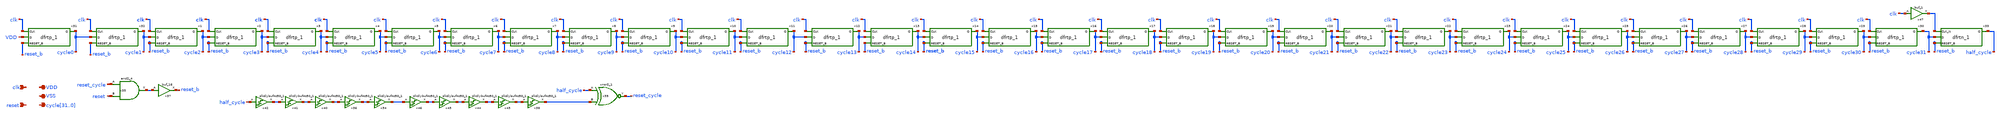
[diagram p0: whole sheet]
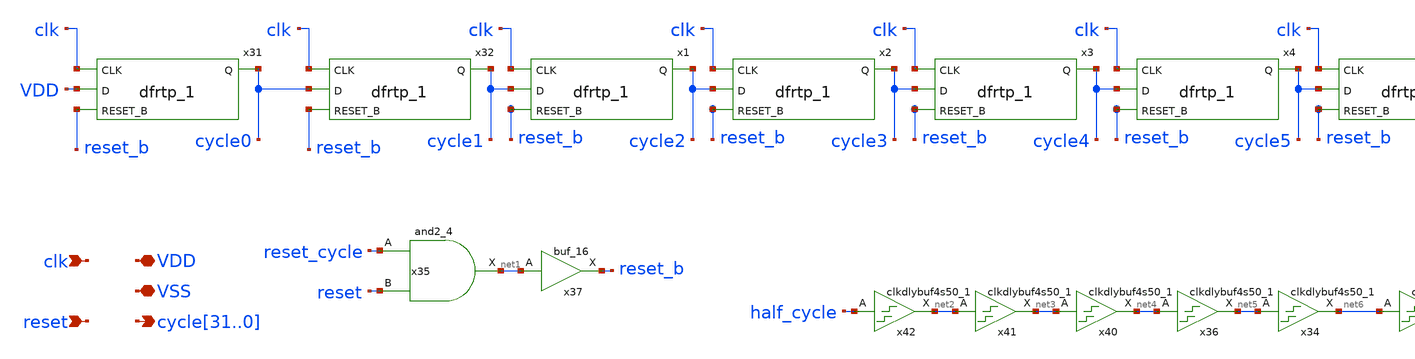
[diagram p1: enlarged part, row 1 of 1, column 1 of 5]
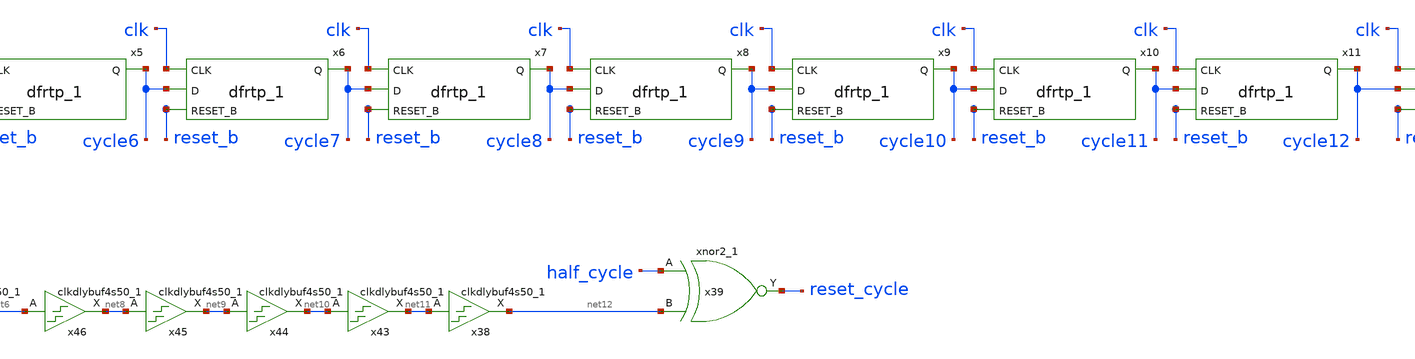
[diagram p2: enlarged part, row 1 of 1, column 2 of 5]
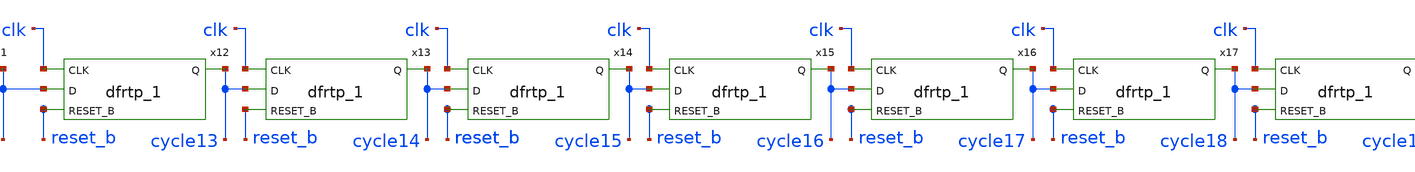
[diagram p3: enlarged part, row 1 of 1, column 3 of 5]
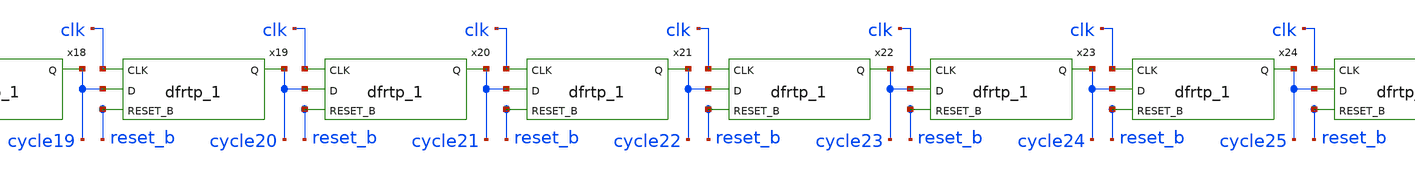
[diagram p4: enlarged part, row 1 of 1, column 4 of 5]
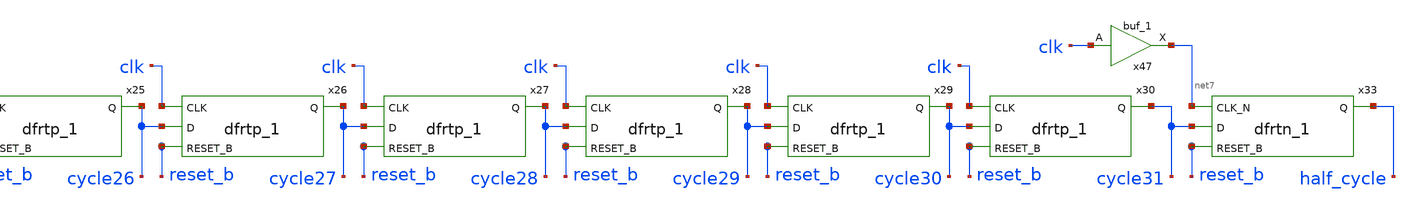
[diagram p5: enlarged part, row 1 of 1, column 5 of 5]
** sch_path: xschem/src/shifted_clock_generator/shifted_clock_generator.sch
**.subckt shifted_clock_generator
*+ cycle31,cycle30,cycle29,cycle28,cycle27,cycle26,cycle25,cycle24,cycle23,cycle22,cycle21,cycle20,cycle19,cycle18,cycle17,cycle16,cycle15,cycle14,cycle13,cycle12,cycle11,cycle10,cycle9,cycle8,cycle7,cycle6,cycle5,cycle4,cycle3,cycle2,cycle1,cycle0 VSS VDD clk reset
*.opin
*+ cycle31,cycle30,cycle29,cycle28,cycle27,cycle26,cycle25,cycle24,cycle23,cycle22,cycle21,cycle20,cycle19,cycle18,cycle17,cycle16,cycle15,cycle14,cycle13,cycle12,cycle11,cycle10,cycle9,cycle8,cycle7,cycle6,cycle5,cycle4,cycle3,cycle2,cycle1,cycle0
*.iopin VSS
*.iopin VDD
*.ipin clk
*.ipin reset
x32 clk cycle0 reset_b VSS VSS VDD VDD cycle1 sky130_fd_sc_hd__dfrtp_1
x1 clk cycle1 reset_b VSS VSS VDD VDD cycle2 sky130_fd_sc_hd__dfrtp_1
x2 clk cycle2 reset_b VSS VSS VDD VDD cycle3 sky130_fd_sc_hd__dfrtp_1
x3 clk cycle3 reset_b VSS VSS VDD VDD cycle4 sky130_fd_sc_hd__dfrtp_1
x4 clk cycle4 reset_b VSS VSS VDD VDD cycle5 sky130_fd_sc_hd__dfrtp_1
x5 clk cycle5 reset_b VSS VSS VDD VDD cycle6 sky130_fd_sc_hd__dfrtp_1
x6 clk cycle6 reset_b VSS VSS VDD VDD cycle7 sky130_fd_sc_hd__dfrtp_1
x7 clk cycle7 reset_b VSS VSS VDD VDD cycle8 sky130_fd_sc_hd__dfrtp_1
x8 clk cycle8 reset_b VSS VSS VDD VDD cycle9 sky130_fd_sc_hd__dfrtp_1
x9 clk cycle9 reset_b VSS VSS VDD VDD cycle10 sky130_fd_sc_hd__dfrtp_1
x10 clk cycle10 reset_b VSS VSS VDD VDD cycle11 sky130_fd_sc_hd__dfrtp_1
x11 clk cycle11 reset_b VSS VSS VDD VDD cycle12 sky130_fd_sc_hd__dfrtp_1
x12 clk cycle12 reset_b VSS VSS VDD VDD cycle13 sky130_fd_sc_hd__dfrtp_1
x13 clk cycle13 reset_b VSS VSS VDD VDD cycle14 sky130_fd_sc_hd__dfrtp_1
x14 clk cycle14 reset_b VSS VSS VDD VDD cycle15 sky130_fd_sc_hd__dfrtp_1
x15 clk cycle15 reset_b VSS VSS VDD VDD cycle16 sky130_fd_sc_hd__dfrtp_1
x16 clk cycle16 reset_b VSS VSS VDD VDD cycle17 sky130_fd_sc_hd__dfrtp_1
x17 clk cycle17 reset_b VSS VSS VDD VDD cycle18 sky130_fd_sc_hd__dfrtp_1
x18 clk cycle18 reset_b VSS VSS VDD VDD cycle19 sky130_fd_sc_hd__dfrtp_1
x19 clk cycle19 reset_b VSS VSS VDD VDD cycle20 sky130_fd_sc_hd__dfrtp_1
x20 clk cycle20 reset_b VSS VSS VDD VDD cycle21 sky130_fd_sc_hd__dfrtp_1
x21 clk cycle21 reset_b VSS VSS VDD VDD cycle22 sky130_fd_sc_hd__dfrtp_1
x22 clk cycle22 reset_b VSS VSS VDD VDD cycle23 sky130_fd_sc_hd__dfrtp_1
x23 clk cycle23 reset_b VSS VSS VDD VDD cycle24 sky130_fd_sc_hd__dfrtp_1
x24 clk cycle24 reset_b VSS VSS VDD VDD cycle25 sky130_fd_sc_hd__dfrtp_1
x25 clk cycle25 reset_b VSS VSS VDD VDD cycle26 sky130_fd_sc_hd__dfrtp_1
x26 clk cycle26 reset_b VSS VSS VDD VDD cycle27 sky130_fd_sc_hd__dfrtp_1
x27 clk cycle27 reset_b VSS VSS VDD VDD cycle28 sky130_fd_sc_hd__dfrtp_1
x28 clk cycle28 reset_b VSS VSS VDD VDD cycle29 sky130_fd_sc_hd__dfrtp_1
x29 clk cycle29 reset_b VSS VSS VDD VDD cycle30 sky130_fd_sc_hd__dfrtp_1
x30 clk cycle30 reset_b VSS VSS VDD VDD cycle31 sky130_fd_sc_hd__dfrtp_1
x31 clk VDD reset_b VSS VSS VDD VDD cycle0 sky130_fd_sc_hd__dfrtp_1
x37 net1 VSS VSS VDD VDD reset_b sky130_fd_sc_hd__buf_16
x35 reset_cycle reset VSS VSS VDD VDD net1 sky130_fd_sc_hd__and2_4
x34 net5 VSS VSS VDD VDD net6 sky130_fd_sc_hd__clkdlybuf4s50_1
x39 half_cycle net12 VSS VSS VDD VDD reset_cycle sky130_fd_sc_hd__xnor2_1
x36 net4 VSS VSS VDD VDD net5 sky130_fd_sc_hd__clkdlybuf4s50_1
x40 net3 VSS VSS VDD VDD net4 sky130_fd_sc_hd__clkdlybuf4s50_1
x41 net2 VSS VSS VDD VDD net3 sky130_fd_sc_hd__clkdlybuf4s50_1
x42 half_cycle VSS VSS VDD VDD net2 sky130_fd_sc_hd__clkdlybuf4s50_1
x33 net7 cycle31 reset_b VSS VSS VDD VDD half_cycle sky130_fd_sc_hd__dfrtn_1
x38 net11 VSS VSS VDD VDD net12 sky130_fd_sc_hd__clkdlybuf4s50_1
x43 net10 VSS VSS VDD VDD net11 sky130_fd_sc_hd__clkdlybuf4s50_1
x44 net9 VSS VSS VDD VDD net10 sky130_fd_sc_hd__clkdlybuf4s50_1
x45 net8 VSS VSS VDD VDD net9 sky130_fd_sc_hd__clkdlybuf4s50_1
x46 net6 VSS VSS VDD VDD net8 sky130_fd_sc_hd__clkdlybuf4s50_1
x47 clk VSS VSS VDD VDD net7 sky130_fd_sc_hd__buf_1
**.ends
.end
